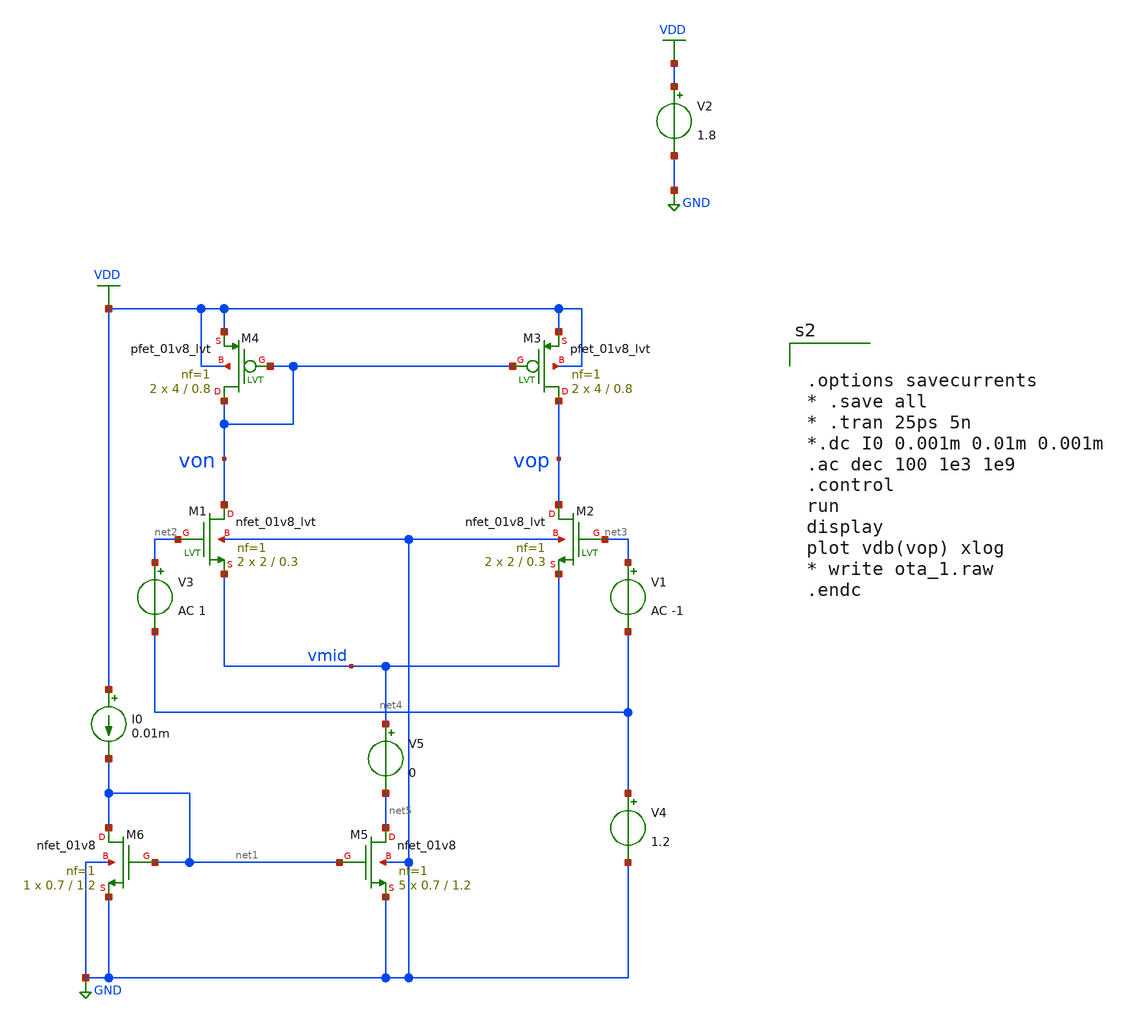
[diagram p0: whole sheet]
** sch_path: xschem/ota_1.sch
**.subckt ota_1
V2 VDD GND 1.8
XM1 von net2 vmid GND sky130_fd_pr__nfet_01v8_lvt L=0.3 W=2 nf=1 ad='int((nf+1)/2) * W/nf * 0.29' as='int((nf+2)/2) * W/nf * 0.29'
+ pd='2*int((nf+1)/2) * (W/nf + 0.29)' ps='2*int((nf+2)/2) * (W/nf + 0.29)' nrd='0.29 / W' nrs='0.29 / W'
+ sa=0 sb=0 sd=0 mult=2 m=2
XM2 vop net3 vmid GND sky130_fd_pr__nfet_01v8_lvt L=0.3 W=2 nf=1 ad='int((nf+1)/2) * W/nf * 0.29' as='int((nf+2)/2) * W/nf * 0.29'
+ pd='2*int((nf+1)/2) * (W/nf + 0.29)' ps='2*int((nf+2)/2) * (W/nf + 0.29)' nrd='0.29 / W' nrs='0.29 / W'
+ sa=0 sb=0 sd=0 mult=2 m=2
XM3 vop von VDD VDD sky130_fd_pr__pfet_01v8_lvt L=0.8 W=4 nf=1 ad='int((nf+1)/2) * W/nf * 0.29' as='int((nf+2)/2) * W/nf * 0.29'
+ pd='2*int((nf+1)/2) * (W/nf + 0.29)' ps='2*int((nf+2)/2) * (W/nf + 0.29)' nrd='0.29 / W' nrs='0.29 / W'
+ sa=0 sb=0 sd=0 mult=2 m=2
XM4 von von VDD VDD sky130_fd_pr__pfet_01v8_lvt L=0.8 W=4 nf=1 ad='int((nf+1)/2) * W/nf * 0.29' as='int((nf+2)/2) * W/nf * 0.29'
+ pd='2*int((nf+1)/2) * (W/nf + 0.29)' ps='2*int((nf+2)/2) * (W/nf + 0.29)' nrd='0.29 / W' nrs='0.29 / W'
+ sa=0 sb=0 sd=0 mult=2 m=2
XM5 net5 net1 GND GND sky130_fd_pr__nfet_01v8 L=1.2 W=0.7 nf=1 ad='int((nf+1)/2) * W/nf * 0.29' as='int((nf+2)/2) * W/nf * 0.29'
+ pd='2*int((nf+1)/2) * (W/nf + 0.29)' ps='2*int((nf+2)/2) * (W/nf + 0.29)' nrd='0.29 / W' nrs='0.29 / W'
+ sa=0 sb=0 sd=0 mult=5 m=5
XM6 net1 net1 GND GND sky130_fd_pr__nfet_01v8 L=1.2 W=0.7 nf=1 ad='int((nf+1)/2) * W/nf * 0.29' as='int((nf+2)/2) * W/nf * 0.29'
+ pd='2*int((nf+1)/2) * (W/nf + 0.29)' ps='2*int((nf+2)/2) * (W/nf + 0.29)' nrd='0.29 / W' nrs='0.29 / W'
+ sa=0 sb=0 sd=0 mult=1 m=1
I0 VDD net1 0.01m
V1 net3 net4 AC -1
V3 net2 net4 AC 1
V4 net4 GND 1.2
V5 vmid net5 0
**** begin user architecture code
.lib $::SKYWATER_MODELS/sky130.lib.spice tt
* .include $::PDKPATH/libs.ref/sky130_fd_sc_hvl/spice/sky130_fd_sc_hvl.spice



.options savecurrents
* .save all
* .tran 25ps 5n
*.dc I0 0.001m 0.01m 0.001m
.ac dec 100 1e3 1e9
.control
run
display
plot vdb(vop) xlog
* write ota_1.raw
.endc


**** end user architecture code
**.ends
.GLOBAL VDD
.GLOBAL GND
.end
